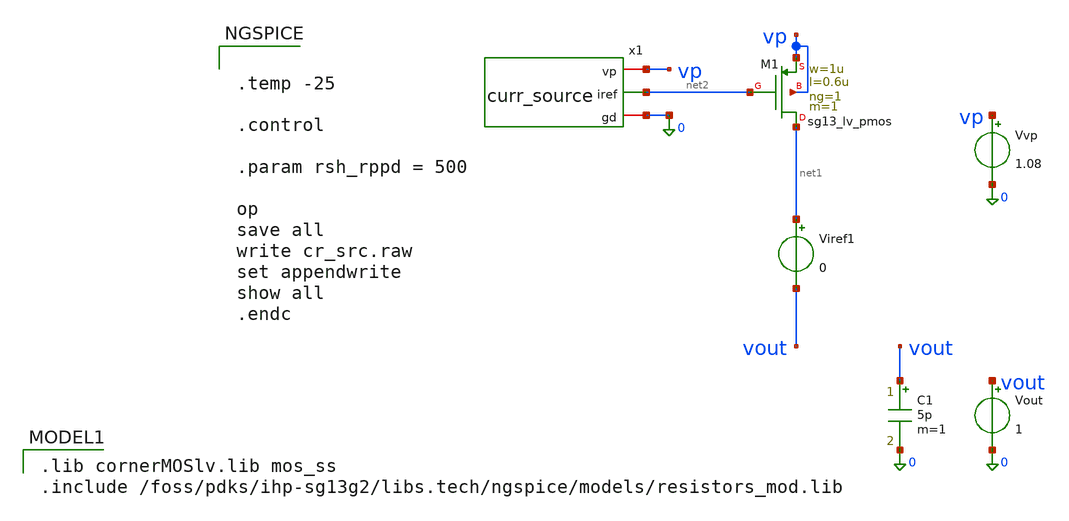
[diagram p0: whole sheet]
** sch_path: schematics/charge_pump/curr_source_tb.sch
**.subckt curr_source_tb
Vvp vp 0 1.08
Viref1 net1 vout 0
XM1 net1 net2 vp vp sg13_lv_pmos w=1u l=0.6u ng=1 m=1 mm_ok=1
C1 vout 0 5p m=1
Vout vout 0 1
x1 vp net2 0 curr_source
**** begin user architecture code


.temp -25

.control

.param rsh_rppd = 500

op
save all
write cr_src.raw
set appendwrite
show all
.endc


 .lib cornerMOSlv.lib mos_ss
.include /foss/pdks/ihp-sg13g2/libs.tech/ngspice/models/resistors_mod.lib

**** end user architecture code
**.ends

* expanding   symbol:  /foss/designs/CHIP-PLL/charge_pump/curr_source.sym # of pins=3
** sym_path: charge_pump/curr_source.sym
** sch_path: charge_pump/curr_source.sch
.subckt curr_source vp iref gd
*.iopin vp
*.iopin gd
*.opin iref
XM4 iref iref vp vp sg13_lv_pmos w=1.4u l=0.6u ng=1 m=1 mm_ok=1
XM5 net2 iref vp vp sg13_lv_pmos w=1.2u l=0.6u ng=1 m=1 mm_ok=1
XM6 net3 net3 gd gd sg13_lv_nmos w=1u l=0.6u ng=1 m=1 mm_ok=1
XM3 net2 net2 gd gd sg13_lv_nmos w=1.4u l=0.6u ng=1 m=1 mm_ok=1
XR2 net1 gd gd rppd w=1e-6 l=1.70e-6 m=1 b=0 mm_ok=1
XM1 iref net2 net1 gd sg13_lv_nmos w=1.2u l=0.6u ng=1 m=1 mm_ok=1
XM2 vp net3 iref gd sg13_lv_nmos w=1u l=0.6u ng=1 m=1 mm_ok=1
XM7 vp vp net3 gd sg13_lv_nmos w=1u l=0.6u ng=1 m=1 mm_ok=1
XM8 gd gd gd gd sg13_lv_nmos w=0.4u l=0.6u ng=1 m=1 mm_ok=1
.ends

.end
